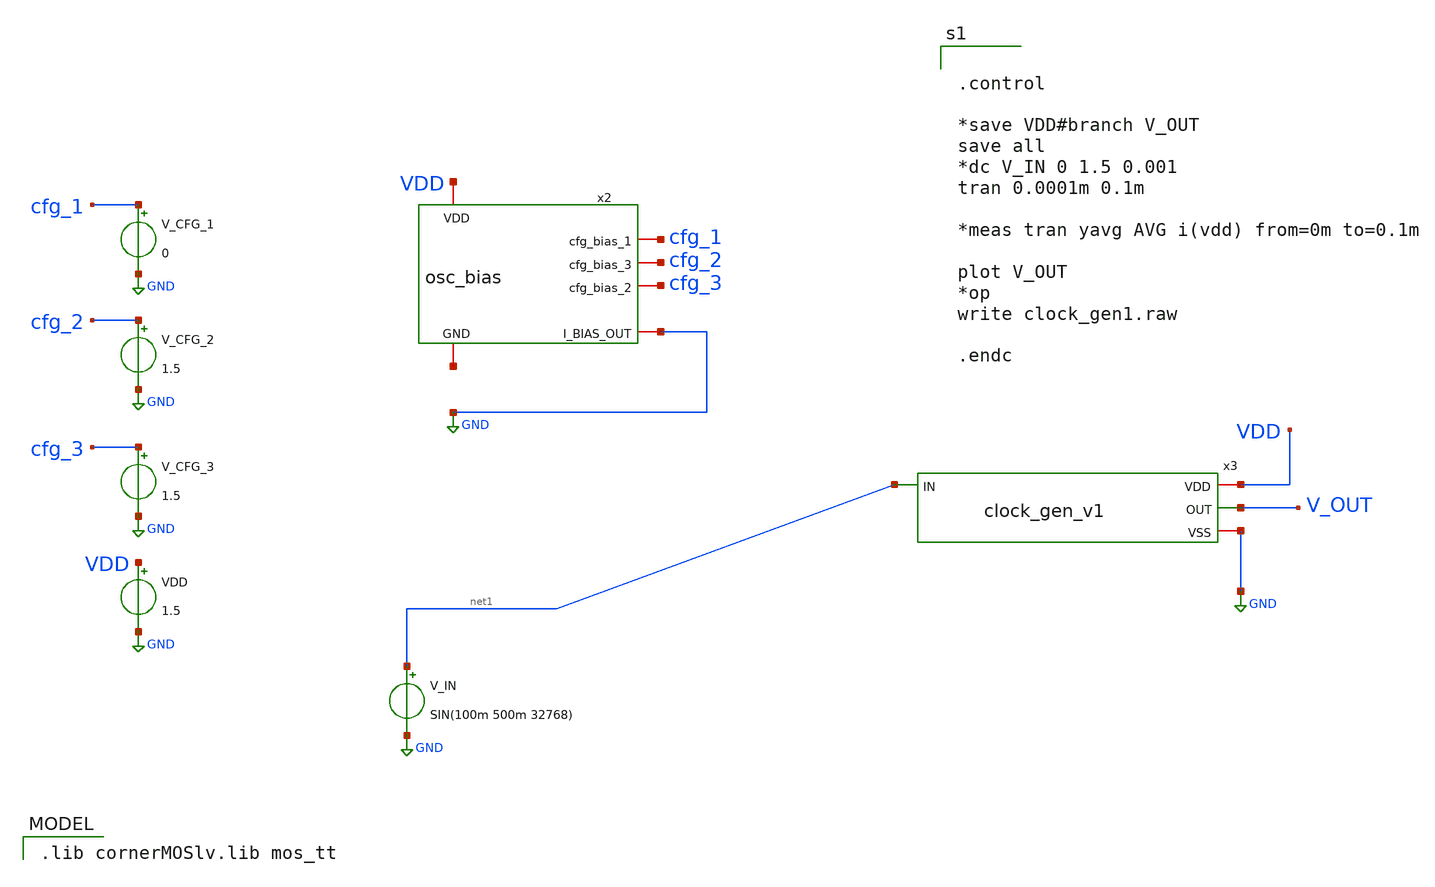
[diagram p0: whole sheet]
** sch_path: clock_gen_tb_1.sch
**.subckt clock_gen_tb_1
VDD VDD GND 1.5
V_IN net1 GND SIN(100m 500m 32768)
x2 VDD cfg_1 cfg_2 cfg_3 net2 GND osc_bias
V_CFG_1 cfg_1 GND 0
V_CFG_2 cfg_2 GND 1.5
V_CFG_3 cfg_3 GND 1.5
x3 VDD net1 V_OUT GND clock_gen_v1
**** begin user architecture code
 .lib cornerMOSlv.lib mos_tt



.control

*save VDD#branch V_OUT
save all
*dc V_IN 0 1.5 0.001
tran 0.0001m 0.1m

*meas tran yavg AVG i(vdd) from=0m to=0.1m

plot V_OUT
*op
write clock_gen1.raw

.endc


**** end user architecture code
**.ends

* expanding   symbol:  osc_bias.sym # of pins=6
** sym_path: osc_bias.sym
** sch_path: osc_bias.sch
.subckt osc_bias VDD cfg_bias_1 cfg_bias_3 cfg_bias_2 GND I_BIAS_OUT
*.iopin VDD
*.iopin GND
*.iopin I_BIAS_OUT
*.iopin cfg_bias_1
*.iopin cfg_bias_2
*.iopin cfg_bias_3
XM1 vp_bias vp_bias VDD VDD sg13_lv_pmos w=1u l=10u ng=1 m=1 mm_ok=1
XM3 vp_bias vp_bias net2 net1 sg13_lv_nmos w=0.25u l=10u ng=1 m=1 mm_ok=1
XM4 net2 net2 net3 net1 sg13_lv_nmos w=0.25u l=10u ng=1 m=1 mm_ok=1
XM5 net3 net3 net1 net1 sg13_lv_nmos w=0.25u l=10u ng=1 m=1 mm_ok=1
XM2 net7 vp_bias VDD VDD sg13_lv_pmos w=0.5u l=10u ng=1 m=1 mm_ok=1
XM6 I_BIAS_OUT cfg_bias_1 net7 VDD sg13_lv_pmos w=0.5u l=5u ng=1 m=1 mm_ok=1
XM7 net4 vp_bias VDD VDD sg13_lv_pmos w=0.5u l=10u ng=1 m=1 mm_ok=1
XM8 net5 vp_bias VDD VDD sg13_lv_pmos w=0.5u l=10u ng=1 m=1 mm_ok=1
XM9 I_BIAS_OUT cfg_bias_2 net4 VDD sg13_lv_pmos w=0.5u l=10u ng=1 m=1 mm_ok=1
XM10 I_BIAS_OUT cfg_bias_3 net5 VDD sg13_lv_pmos w=0.5u l=10u ng=1 m=1 mm_ok=1
XM11 net1 net1 net6 net1 sg13_lv_nmos w=0.25u l=10u ng=1 m=1 mm_ok=1
Vmeas net6 GND 0
.save i(vmeas)
.ends


* expanding   symbol:  clock_gen_v1.sym # of pins=4
** sym_path: clock_gen_v1.sym
** sch_path: clock_gen_v1.sch
.subckt clock_gen_v1 VDD IN OUT VSS
*.iopin VSS
*.iopin VDD
*.ipin IN
*.opin OUT
XM1 stage_1 net1 net2 VSS sg13_lv_nmos w=1u l=0.13u ng=1 m=1 mm_ok=1
XM2 stage_1 net1 net3 VDD sg13_lv_pmos w=2u l=0.13u ng=1 m=1 mm_ok=1
R1 stage_1 net1 1G m=1
C1 IN net1 10p m=1
XM3 stage_2 stage_1 VSS VSS sg13_lv_nmos w=1u l=0.13u ng=1 m=1 mm_ok=1
XM4 stage_2 stage_1 VDD VDD sg13_lv_pmos w=1u l=0.13u ng=1 m=1 mm_ok=1
XM5 OUT stage_2 VSS VSS sg13_lv_nmos w=1u l=0.13u ng=1 m=1 mm_ok=1
XM6 OUT stage_2 VDD VDD sg13_lv_pmos w=1u l=0.13u ng=1 m=1 mm_ok=1
Vmeas_NMOS net2 VSS 0
.save i(vmeas_nmos)
Vmeas_PMOS net4 net3 0
.save i(vmeas_pmos)
.ends

.GLOBAL GND
.end
